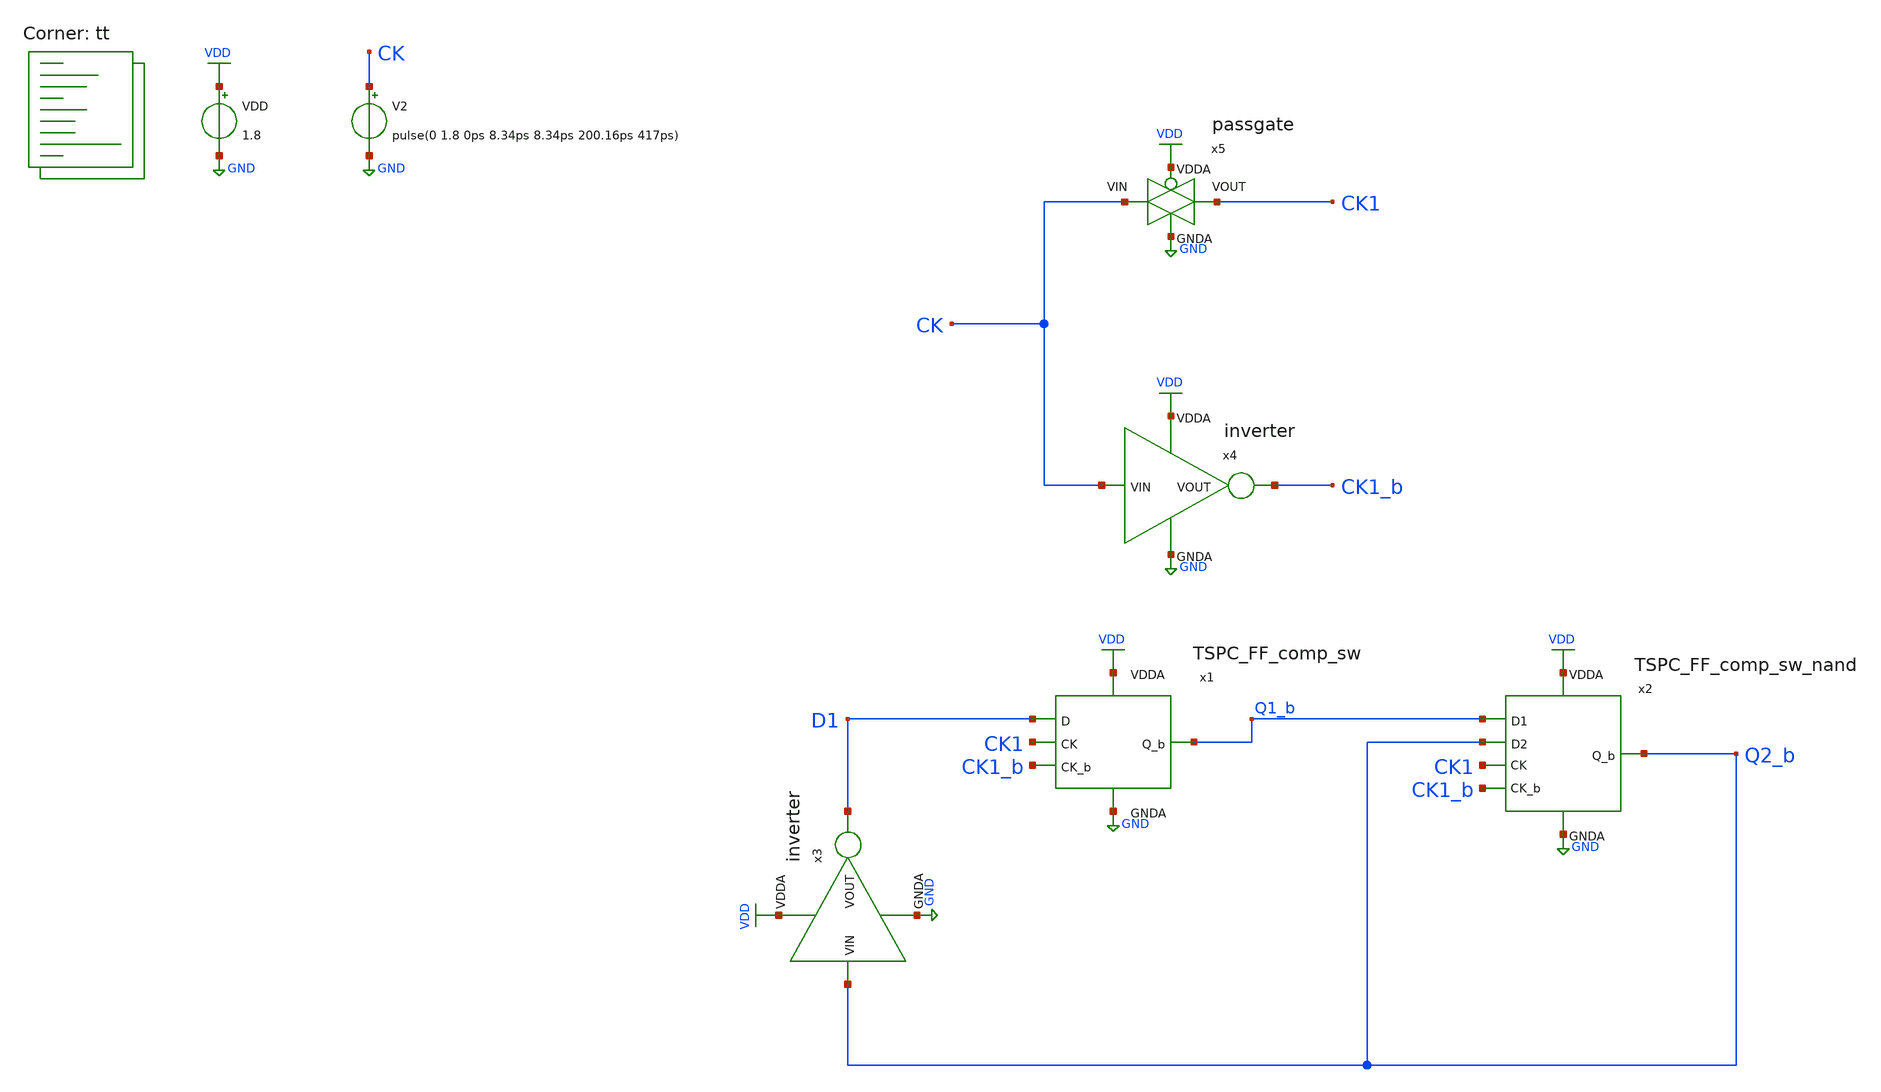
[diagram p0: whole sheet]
** sch_path: projects/pll/divider/xschem_ngspice/tb_TSPC_FF_comp_sw_divide3_7.sch
**.subckt tb_TSPC_FF_comp_sw_divide3_7
VDD VDD GND 1.8
V2 CK GND pulse(0 1.8 0ps 8.34ps 8.34ps 200.16ps 417ps)
x3 VDD Q2_b D1 GND inverter
x2 VDD Q2_b Q2_b Q1_b CK1_b CK1 GND TSPC_FF_comp_sw_nand
x1 VDD Q1_b D1 CK1_b GND CK1 TSPC_FF_comp_sw
x4 VDD CK CK1_b GND inverter
x5 VDD CK CK1 GND passgate
**** begin user architecture code



.include /foss/pdks/sky130A/libs.ref/sky130_fd_sc_hd/spice/sky130_fd_sc_hd.spice

.option method=gear
.option wnflag=1
.option savecurrents

.save @m.xm1.msky130_fd_pr__pfet_01v8[gm] @m.xm2.msky130_fd_pr__nfet_01v8[gm] @m.xm3.msky130_fd_pr__pfet_01v8[gm] @m.xm4.msky130_fd_pr__nfet_01v8[gm] @m.xm4_c.msky130_fd_pr__pfet_01v8[gm] @m.xm5.msky130_fd_pr__nfet_01v8[gm] @m.xm6.msky130_fd_pr__pfet_01v8[gm] @m.xm7.msky130_fd_pr__pfet_01v8[gm] @m.xm7_c.msky130_fd_pr__nfet_01v8[gm] @m.xm8.msky130_fd_pr__nfet_01v8[gm]

*.ic v(d)=0
*.ic v(q)=0
*.ic v(q1)=0

.control

  save v(d1) (q1) v(q1_b) v(q2_b) v(ck) v(ck1) v(ck1_b)
  * save all
  * tran 0.1n 1u
  tran 1p 20n

  remzerovec
  write tb_TSPC_FF_comp_sw_divide3_7.raw
  * set appendwrite

.endc



.lib $::SKYWATER_MODELS/sky130.lib.spice tt
**** end user architecture code
**.ends

* expanding   symbol:  /foss/designs/my_design/projects/pll/divider/xschem_ngspice/inverter.sym # of
*+ pins=4
** sym_path: projects/pll/divider/xschem_ngspice/inverter.sym
** sch_path: projects/pll/divider/xschem_ngspice/inverter.sch
.subckt inverter VDDA VIN VOUT GNDA
*.ipin VIN
*.ipin VDDA
*.ipin GNDA
*.opin VOUT
XM31 VOUT VIN VDDA VDDA sky130_fd_pr__pfet_01v8 L=0.15 W=2 nf=2 ad='int((nf+1)/2) * W/nf * 0.29' as='int((nf+2)/2) * W/nf * 0.29'
+ pd='2*int((nf+1)/2) * (W/nf + 0.29)' ps='2*int((nf+2)/2) * (W/nf + 0.29)' nrd='0.29 / W' nrs='0.29 / W'
+ sa=0 sb=0 sd=0 mult=1 m=1
XM32 VOUT VIN GNDA GNDA sky130_fd_pr__nfet_01v8 L=0.15 W=1 nf=1 ad='int((nf+1)/2) * W/nf * 0.29' as='int((nf+2)/2) * W/nf * 0.29'
+ pd='2*int((nf+1)/2) * (W/nf + 0.29)' ps='2*int((nf+2)/2) * (W/nf + 0.29)' nrd='0.29 / W' nrs='0.29 / W'
+ sa=0 sb=0 sd=0 mult=1 m=1
.ends


* expanding   symbol:
*+  /foss/designs/my_design/projects/pll/divider/xschem_ngspice/TSPC_FF_comp_sw_nand.sym # of pins=7
** sym_path: projects/pll/divider/xschem_ngspice/TSPC_FF_comp_sw_nand.sym
** sch_path: projects/pll/divider/xschem_ngspice/TSPC_FF_comp_sw_nand.sch
.subckt TSPC_FF_comp_sw_nand VDDA Q_b D2 D1 CK_b CK GNDA
*.ipin CK
*.ipin D1
*.opin Q_b
*.ipin VDDA
*.ipin GNDA
*.ipin CK_b
*.ipin D2
XM1 Q_b net2 VDDA VDDA sky130_fd_pr__pfet_01v8 L=0.15 W=1 nf=1 ad='int((nf+1)/2) * W/nf * 0.29' as='int((nf+2)/2) * W/nf * 0.29'
+ pd='2*int((nf+1)/2) * (W/nf + 0.29)' ps='2*int((nf+2)/2) * (W/nf + 0.29)' nrd='0.29 / W' nrs='0.29 / W'
+ sa=0 sb=0 sd=0 mult=1 m=1
XM4 net2 CK net1 GNDA sky130_fd_pr__nfet_01v8 L=0.15 W=1 nf=1 ad='int((nf+1)/2) * W/nf * 0.29' as='int((nf+2)/2) * W/nf * 0.29'
+ pd='2*int((nf+1)/2) * (W/nf + 0.29)' ps='2*int((nf+2)/2) * (W/nf + 0.29)' nrd='0.29 / W' nrs='0.29 / W'
+ sa=0 sb=0 sd=0 mult=1 m=1
XM2 Q_b net1 GNDA GNDA sky130_fd_pr__nfet_01v8 L=0.15 W=1 nf=1 ad='int((nf+1)/2) * W/nf * 0.29' as='int((nf+2)/2) * W/nf * 0.29'
+ pd='2*int((nf+1)/2) * (W/nf + 0.29)' ps='2*int((nf+2)/2) * (W/nf + 0.29)' nrd='0.29 / W' nrs='0.29 / W'
+ sa=0 sb=0 sd=0 mult=1 m=1
XM3 net2 net4 VDDA VDDA sky130_fd_pr__pfet_01v8 L=0.15 W=1 nf=1 ad='int((nf+1)/2) * W/nf * 0.29' as='int((nf+2)/2) * W/nf * 0.29'
+ pd='2*int((nf+1)/2) * (W/nf + 0.29)' ps='2*int((nf+2)/2) * (W/nf + 0.29)' nrd='0.29 / W' nrs='0.29 / W'
+ sa=0 sb=0 sd=0 mult=1 m=1
XM5 net1 net3 GNDA GNDA sky130_fd_pr__nfet_01v8 L=0.15 W=1 nf=1 ad='int((nf+1)/2) * W/nf * 0.29' as='int((nf+2)/2) * W/nf * 0.29'
+ pd='2*int((nf+1)/2) * (W/nf + 0.29)' ps='2*int((nf+2)/2) * (W/nf + 0.29)' nrd='0.29 / W' nrs='0.29 / W'
+ sa=0 sb=0 sd=0 mult=1 m=1
XM6 net4 D2 VDDA VDDA sky130_fd_pr__pfet_01v8 L=0.15 W=1 nf=1 ad='int((nf+1)/2) * W/nf * 0.29' as='int((nf+2)/2) * W/nf * 0.29'
+ pd='2*int((nf+1)/2) * (W/nf + 0.29)' ps='2*int((nf+2)/2) * (W/nf + 0.29)' nrd='0.29 / W' nrs='0.29 / W'
+ sa=0 sb=0 sd=0 mult=1 m=1
XM10 net5 D1 GNDA GNDA sky130_fd_pr__nfet_01v8 L=0.15 W=1 nf=1 ad='int((nf+1)/2) * W/nf * 0.29' as='int((nf+2)/2) * W/nf * 0.29'
+ pd='2*int((nf+1)/2) * (W/nf + 0.29)' ps='2*int((nf+2)/2) * (W/nf + 0.29)' nrd='0.29 / W' nrs='0.29 / W'
+ sa=0 sb=0 sd=0 mult=1 m=1
XM8 net3 CK net4 VDDA sky130_fd_pr__pfet_01v8 L=0.15 W=1 nf=1 ad='int((nf+1)/2) * W/nf * 0.29' as='int((nf+2)/2) * W/nf * 0.29'
+ pd='2*int((nf+1)/2) * (W/nf + 0.29)' ps='2*int((nf+2)/2) * (W/nf + 0.29)' nrd='0.29 / W' nrs='0.29 / W'
+ sa=0 sb=0 sd=0 mult=1 m=1
XM4_c net1 CK_b net2 VDDA sky130_fd_pr__pfet_01v8 L=0.15 W=1 nf=1 ad='int((nf+1)/2) * W/nf * 0.29' as='int((nf+2)/2) * W/nf * 0.29'
+ pd='2*int((nf+1)/2) * (W/nf + 0.29)' ps='2*int((nf+2)/2) * (W/nf + 0.29)' nrd='0.29 / W' nrs='0.29 / W'
+ sa=0 sb=0 sd=0 mult=1 m=1
XM8_c net4 CK_b net3 GNDA sky130_fd_pr__nfet_01v8 L=0.15 W=1 nf=1 ad='int((nf+1)/2) * W/nf * 0.29' as='int((nf+2)/2) * W/nf * 0.29'
+ pd='2*int((nf+1)/2) * (W/nf + 0.29)' ps='2*int((nf+2)/2) * (W/nf + 0.29)' nrd='0.29 / W' nrs='0.29 / W'
+ sa=0 sb=0 sd=0 mult=1 m=1
XM9 net3 D2 net5 GNDA sky130_fd_pr__nfet_01v8 L=0.15 W=1 nf=1 ad='int((nf+1)/2) * W/nf * 0.29' as='int((nf+2)/2) * W/nf * 0.29'
+ pd='2*int((nf+1)/2) * (W/nf + 0.29)' ps='2*int((nf+2)/2) * (W/nf + 0.29)' nrd='0.29 / W' nrs='0.29 / W'
+ sa=0 sb=0 sd=0 mult=1 m=1
XM7 net4 D1 VDDA VDDA sky130_fd_pr__pfet_01v8 L=0.15 W=1 nf=1 ad='int((nf+1)/2) * W/nf * 0.29' as='int((nf+2)/2) * W/nf * 0.29'
+ pd='2*int((nf+1)/2) * (W/nf + 0.29)' ps='2*int((nf+2)/2) * (W/nf + 0.29)' nrd='0.29 / W' nrs='0.29 / W'
+ sa=0 sb=0 sd=0 mult=1 m=1
.ends


* expanding   symbol:
*+  /foss/designs/my_design/projects/pll/divider/xschem_ngspice/TSPC_FF_comp_sw.sym # of pins=6
** sym_path: projects/pll/divider/xschem_ngspice/TSPC_FF_comp_sw.sym
** sch_path: projects/pll/divider/xschem_ngspice/TSPC_FF_comp_sw.sch
.subckt TSPC_FF_comp_sw VDDA Q_b D CK_b GNDA CK
*.ipin CK
*.ipin D
*.opin Q_b
*.ipin VDDA
*.ipin GNDA
*.ipin CK_b
XM1 Q_b net1 VDDA VDDA sky130_fd_pr__pfet_01v8 L=0.15 W=1 nf=1 ad='int((nf+1)/2) * W/nf * 0.29' as='int((nf+2)/2) * W/nf * 0.29'
+ pd='2*int((nf+1)/2) * (W/nf + 0.29)' ps='2*int((nf+2)/2) * (W/nf + 0.29)' nrd='0.29 / W' nrs='0.29 / W'
+ sa=0 sb=0 sd=0 mult=1 m=1
XM4 net1 CK net2 GNDA sky130_fd_pr__nfet_01v8 L=0.15 W=1 nf=1 ad='int((nf+1)/2) * W/nf * 0.29' as='int((nf+2)/2) * W/nf * 0.29'
+ pd='2*int((nf+1)/2) * (W/nf + 0.29)' ps='2*int((nf+2)/2) * (W/nf + 0.29)' nrd='0.29 / W' nrs='0.29 / W'
+ sa=0 sb=0 sd=0 mult=1 m=1
XM2 Q_b net2 GNDA GNDA sky130_fd_pr__nfet_01v8 L=0.15 W=1 nf=1 ad='int((nf+1)/2) * W/nf * 0.29' as='int((nf+2)/2) * W/nf * 0.29'
+ pd='2*int((nf+1)/2) * (W/nf + 0.29)' ps='2*int((nf+2)/2) * (W/nf + 0.29)' nrd='0.29 / W' nrs='0.29 / W'
+ sa=0 sb=0 sd=0 mult=1 m=1
XM3 net1 net4 VDDA VDDA sky130_fd_pr__pfet_01v8 L=0.15 W=1 nf=1 ad='int((nf+1)/2) * W/nf * 0.29' as='int((nf+2)/2) * W/nf * 0.29'
+ pd='2*int((nf+1)/2) * (W/nf + 0.29)' ps='2*int((nf+2)/2) * (W/nf + 0.29)' nrd='0.29 / W' nrs='0.29 / W'
+ sa=0 sb=0 sd=0 mult=1 m=1
XM5 net2 net3 GNDA GNDA sky130_fd_pr__nfet_01v8 L=0.15 W=1 nf=1 ad='int((nf+1)/2) * W/nf * 0.29' as='int((nf+2)/2) * W/nf * 0.29'
+ pd='2*int((nf+1)/2) * (W/nf + 0.29)' ps='2*int((nf+2)/2) * (W/nf + 0.29)' nrd='0.29 / W' nrs='0.29 / W'
+ sa=0 sb=0 sd=0 mult=1 m=1
XM6 net4 D VDDA VDDA sky130_fd_pr__pfet_01v8 L=0.15 W=1 nf=1 ad='int((nf+1)/2) * W/nf * 0.29' as='int((nf+2)/2) * W/nf * 0.29'
+ pd='2*int((nf+1)/2) * (W/nf + 0.29)' ps='2*int((nf+2)/2) * (W/nf + 0.29)' nrd='0.29 / W' nrs='0.29 / W'
+ sa=0 sb=0 sd=0 mult=1 m=1
XM8 net3 D GNDA GNDA sky130_fd_pr__nfet_01v8 L=0.15 W=1 nf=1 ad='int((nf+1)/2) * W/nf * 0.29' as='int((nf+2)/2) * W/nf * 0.29'
+ pd='2*int((nf+1)/2) * (W/nf + 0.29)' ps='2*int((nf+2)/2) * (W/nf + 0.29)' nrd='0.29 / W' nrs='0.29 / W'
+ sa=0 sb=0 sd=0 mult=1 m=1
XM7 net3 CK net4 VDDA sky130_fd_pr__pfet_01v8 L=0.15 W=1 nf=1 ad='int((nf+1)/2) * W/nf * 0.29' as='int((nf+2)/2) * W/nf * 0.29'
+ pd='2*int((nf+1)/2) * (W/nf + 0.29)' ps='2*int((nf+2)/2) * (W/nf + 0.29)' nrd='0.29 / W' nrs='0.29 / W'
+ sa=0 sb=0 sd=0 mult=1 m=1
XM4_c net2 CK_b net1 VDDA sky130_fd_pr__pfet_01v8 L=0.15 W=1 nf=1 ad='int((nf+1)/2) * W/nf * 0.29' as='int((nf+2)/2) * W/nf * 0.29'
+ pd='2*int((nf+1)/2) * (W/nf + 0.29)' ps='2*int((nf+2)/2) * (W/nf + 0.29)' nrd='0.29 / W' nrs='0.29 / W'
+ sa=0 sb=0 sd=0 mult=1 m=1
XM7_c net4 CK_b net3 GNDA sky130_fd_pr__nfet_01v8 L=0.15 W=1 nf=1 ad='int((nf+1)/2) * W/nf * 0.29' as='int((nf+2)/2) * W/nf * 0.29'
+ pd='2*int((nf+1)/2) * (W/nf + 0.29)' ps='2*int((nf+2)/2) * (W/nf + 0.29)' nrd='0.29 / W' nrs='0.29 / W'
+ sa=0 sb=0 sd=0 mult=1 m=1
.ends


* expanding   symbol:  /foss/designs/my_design/projects/pll/divider/xschem_ngspice/passgate.sym # of
*+ pins=4
** sym_path: projects/pll/divider/xschem_ngspice/passgate.sym
** sch_path: projects/pll/divider/xschem_ngspice/passgate.sch
.subckt passgate VDDA VIN VOUT GNDA
*.ipin VDDA
*.ipin GNDA
*.ipin VIN
*.opin VOUT
XM12 VOUT GNDA VIN VDDA sky130_fd_pr__pfet_01v8 L=0.15 W=2 nf=2 ad='int((nf+1)/2) * W/nf * 0.29' as='int((nf+2)/2) * W/nf * 0.29'
+ pd='2*int((nf+1)/2) * (W/nf + 0.29)' ps='2*int((nf+2)/2) * (W/nf + 0.29)' nrd='0.29 / W' nrs='0.29 / W'
+ sa=0 sb=0 sd=0 mult=1 m=1
XM13 VOUT VDDA VIN GNDA sky130_fd_pr__nfet_01v8 L=0.15 W=1 nf=1 ad='int((nf+1)/2) * W/nf * 0.29' as='int((nf+2)/2) * W/nf * 0.29'
+ pd='2*int((nf+1)/2) * (W/nf + 0.29)' ps='2*int((nf+2)/2) * (W/nf + 0.29)' nrd='0.29 / W' nrs='0.29 / W'
+ sa=0 sb=0 sd=0 mult=1 m=1
.ends

.GLOBAL GND
.GLOBAL VDD
.end
